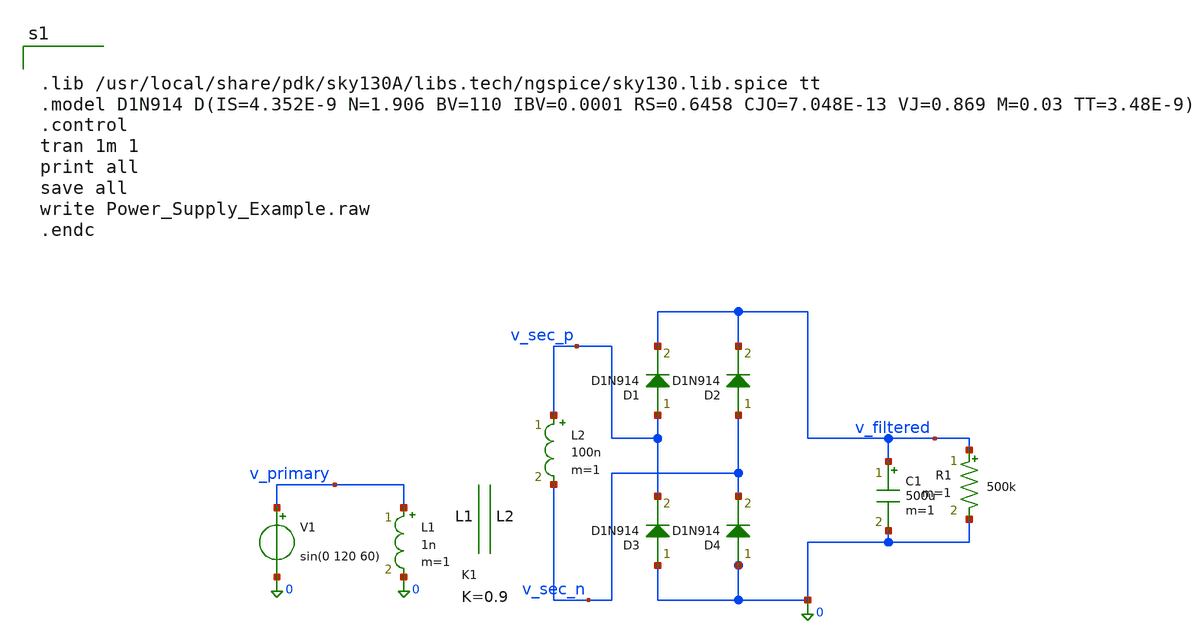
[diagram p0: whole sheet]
** sch_path: mag/Power_Supply_Example.sch
**.subckt Power_Supply_Example
L1 v_primary 0 1n m=1
L2 v_sec_p v_sec_n 100n m=1
K1 L1 L2 0.9
V1 v_primary 0 sin(0 120 60)
D1 v_sec_p v_filtered D1N914 area=1
C1 v_filtered 0 500u m=1
R1 v_filtered 0 500k m=1
D2 v_sec_n v_filtered D1N914 area=1
D3 0 v_sec_p D1N914 area=1
D4 0 v_sec_n D1N914 area=1
**** begin user architecture code


.lib /usr/local/share/pdk/sky130A/libs.tech/ngspice/sky130.lib.spice tt
.model D1N914 D(IS=4.352E-9 N=1.906 BV=110 IBV=0.0001 RS=0.6458 CJO=7.048E-13 VJ=0.869 M=0.03
+ TT=3.48E-9)
.control
tran 1m 1
print all
save all
write Power_Supply_Example.raw
.endc

**** end user architecture code
**.ends
.end
